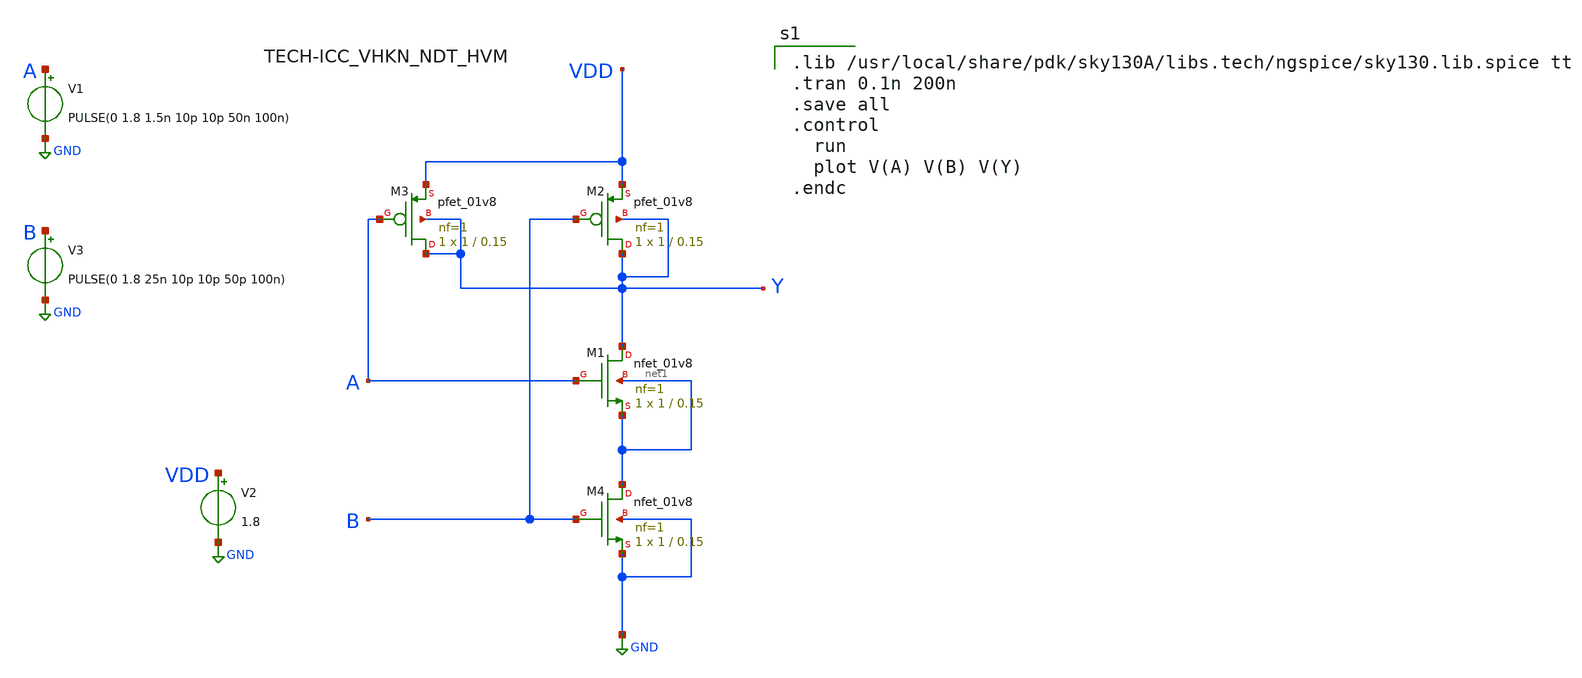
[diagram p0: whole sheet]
** sch_path: CMOS_NAND2_1/CMOS_NAND_SCHEMATIC.sch
**.subckt CMOS_NAND_SCHEMATIC
XM1 Y A net1 net1 sky130_fd_pr__nfet_01v8 L=0.15 W=1 nf=1 ad='int((1 + 1)/2) * 1 / 1 * 0.29' as='int((1 + 2)/2) * 1 / 1 * 0.29'
+ pd='2*int((1 + 1)/2) * (1 / 1 + 0.29)' ps='2*int((1 + 2)/2) * (1 / 1 + 0.29)' nrd='0.29 / 1 ' nrs='0.29 / 1 '
+ sa=0 sb=0 sd=0 mult=1 m=1
XM2 Y B VDD Y sky130_fd_pr__pfet_01v8 L=0.15 W=1 nf=1 ad='int((1 + 1)/2) * 1 / 1 * 0.29' as='int((1 + 2)/2) * 1 / 1 * 0.29'
+ pd='2*int((1 + 1)/2) * (1 / 1 + 0.29)' ps='2*int((1 + 2)/2) * (1 / 1 + 0.29)' nrd='0.29 / 1 ' nrs='0.29 / 1 '
+ sa=0 sb=0 sd=0 mult=1 m=1
XM3 Y A VDD Y sky130_fd_pr__pfet_01v8 L=0.15 W=1 nf=1 ad='int((1 + 1)/2) * 1 / 1 * 0.29' as='int((1 + 2)/2) * 1 / 1 * 0.29'
+ pd='2*int((1 + 1)/2) * (1 / 1 + 0.29)' ps='2*int((1 + 2)/2) * (1 / 1 + 0.29)' nrd='0.29 / 1 ' nrs='0.29 / 1 '
+ sa=0 sb=0 sd=0 mult=1 m=1
XM4 net1 B GND GND sky130_fd_pr__nfet_01v8 L=0.15 W=1 nf=1 ad='int((1 + 1)/2) * 1 / 1 * 0.29' as='int((1 + 2)/2) * 1 / 1 * 0.29'
+ pd='2*int((1 + 1)/2) * (1 / 1 + 0.29)' ps='2*int((1 + 2)/2) * (1 / 1 + 0.29)' nrd='0.29 / 1 ' nrs='0.29 / 1 '
+ sa=0 sb=0 sd=0 mult=1 m=1
V1 A GND PULSE(0 1.8 1.5n 10p 10p 50n 100n)
V2 VDD GND 1.8
V3 B GND PULSE(0 1.8 25n 10p 10p 50p 100n)
**** begin user architecture code

.lib /usr/local/share/pdk/sky130A/libs.tech/ngspice/sky130.lib.spice tt
.tran 0.1n 200n
.save all
.control
  run
  plot V(A) V(B) V(Y)
.endc


**** end user architecture code
**.ends
.GLOBAL GND
.end
